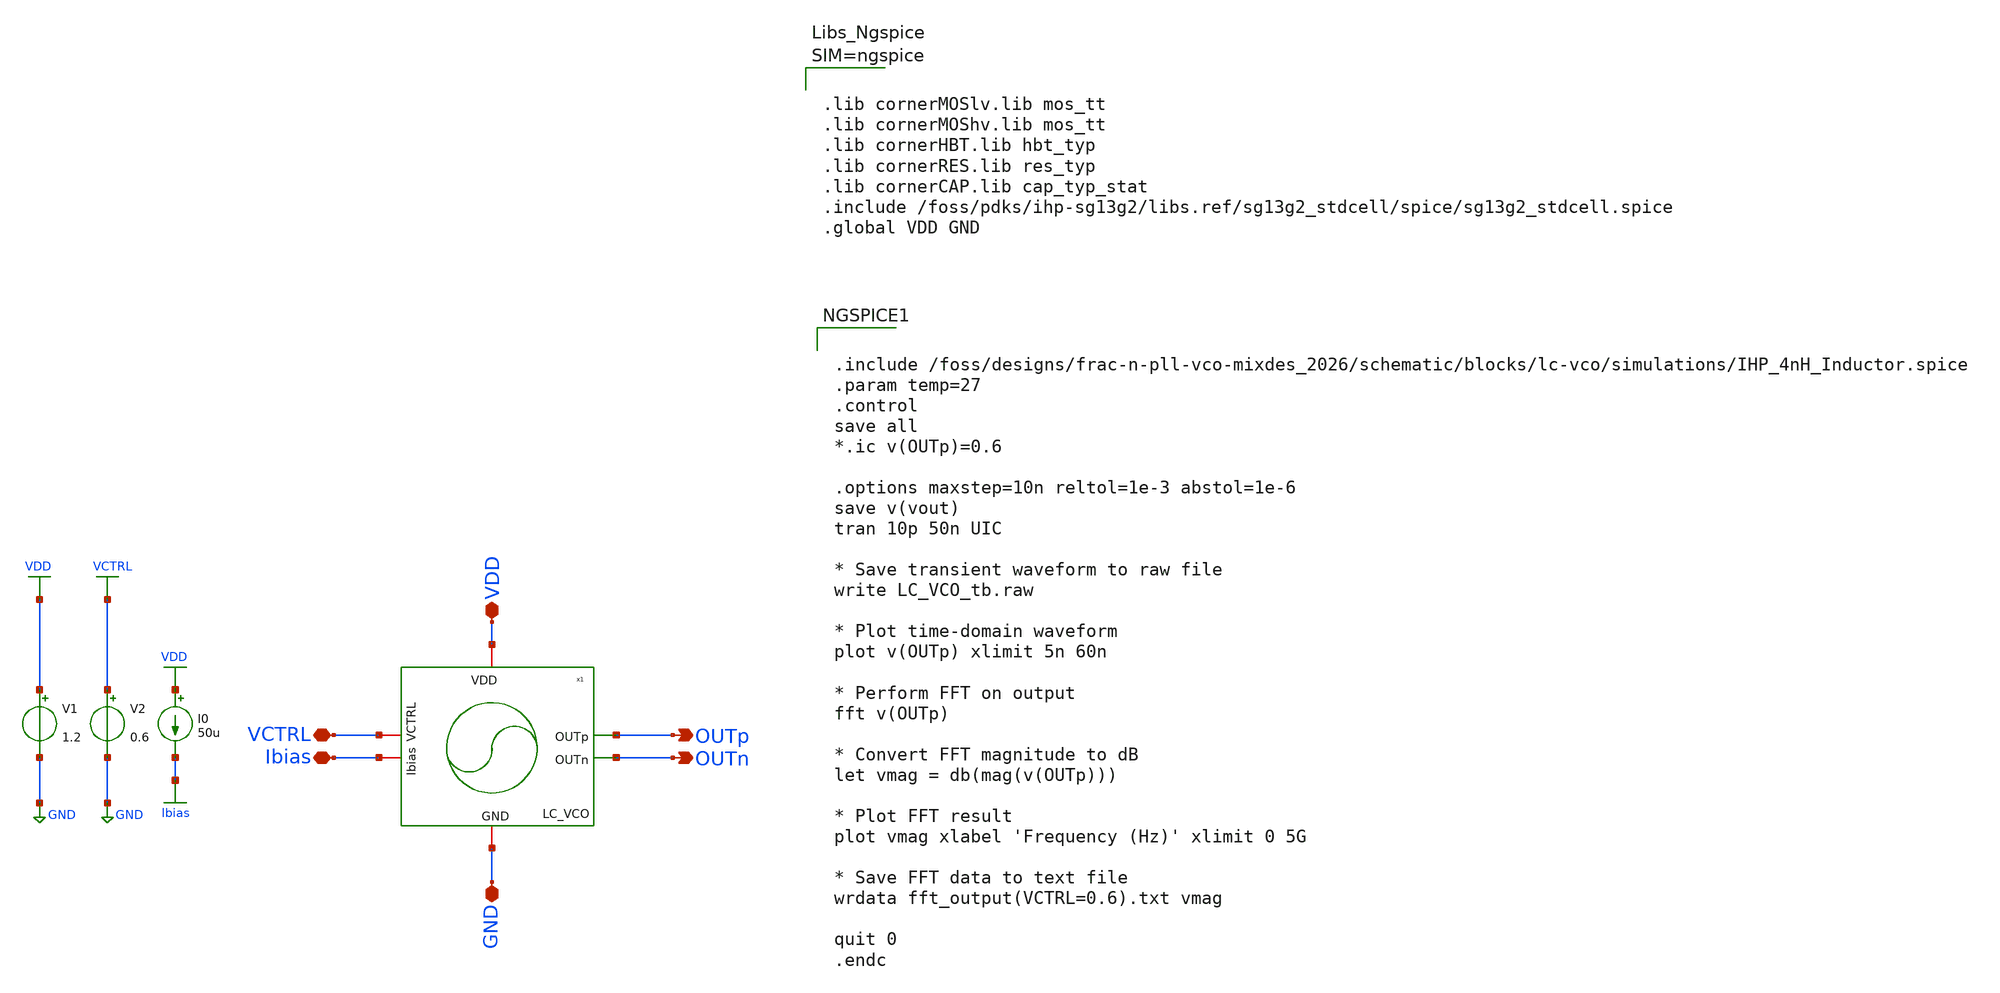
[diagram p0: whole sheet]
** sch_path: tb/tb_VCO.sch
**.subckt tb_VCO OUTp OUTn VDD VCTRL GND Ibias
*.opin OUTp
*.opin OUTn
*.iopin VDD
*.iopin VCTRL
*.iopin GND
*.iopin Ibias
V1 VDD GND 1.2
V2 VCTRL GND 0.6
I0 VDD Ibias 50u
x2 VDD OUTp OUTn Ibias VCTRL GND LC_VCO
**** begin user architecture code


.include /foss/designs/frac-n-pll-vco-mixdes_2026/schematic/blocks/lc-vco/simulations/IHP_4nH_Inductor.spice
.param temp=27
.control
save all
*.ic v(OUTp)=0.6

.options maxstep=10n reltol=1e-3 abstol=1e-6
save v(vout)
tran 10p 50n UIC

* Save transient waveform to raw file
write LC_VCO_tb.raw

* Plot time-domain waveform
plot v(OUTp) xlimit 5n 60n

* Perform FFT on output
fft v(OUTp)

* Convert FFT magnitude to dB
let vmag = db(mag(v(OUTp)))

* Plot FFT result
plot vmag xlabel 'Frequency (Hz)' xlimit 0 5G

* Save FFT data to text file
wrdata fft_output(VCTRL=0.6).txt vmag

quit 0
.endc





.lib cornerMOSlv.lib mos_tt
.lib cornerMOShv.lib mos_tt
.lib cornerHBT.lib hbt_typ
.lib cornerRES.lib res_typ
.lib cornerCAP.lib cap_typ_stat
.include /foss/pdks/ihp-sg13g2/libs.ref/sg13g2_stdcell/spice/sg13g2_stdcell.spice
.global VDD GND




**** end user architecture code
**.ends
.GLOBAL GND
.GLOBAL VDD
.GLOBAL VCTRL
.GLOBAL Ibias
.end
